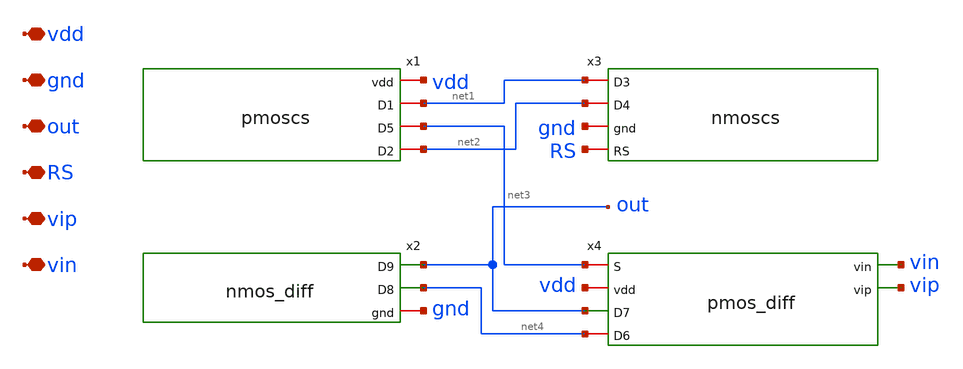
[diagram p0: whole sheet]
** sch_path: op_amp.sch
**.subckt op_amp vdd gnd out RS vip vin
*.iopin vdd
*.iopin gnd
*.iopin out
*.iopin RS
*.iopin vip
*.iopin vin
x1 vdd net1 net3 net2 pmoscs
x2 out net4 gnd nmos_diff
x4 net3 vin vip vdd out net4 pmos_diff
x3 net1 net2 gnd RS nmoscs
**.ends

* expanding   symbol:  pmoscs.sym # of pins=4
** sym_path: pmoscs.sym
** sch_path: pmoscs.sch
.subckt pmoscs vdd D1 D5 D2
*.iopin vdd
*.iopin D1
*.iopin D2
*.iopin D5
XM1 D1 D2 vdd vdd sky130_fd_pr__pfet_01v8 L=1 W=2 nf=1 ad='int((nf+1)/2) * W/nf * 0.29' as='int((nf+2)/2) * W/nf * 0.29'
+ pd='2*int((nf+1)/2) * (W/nf + 0.29)' ps='2*int((nf+2)/2) * (W/nf + 0.29)' nrd='0.29 / W' nrs='0.29 / W'
+ sa=0 sb=0 sd=0 mult=2 m=2
XM2 D2 D2 vdd vdd sky130_fd_pr__pfet_01v8 L=1 W=2 nf=1 ad='int((nf+1)/2) * W/nf * 0.29' as='int((nf+2)/2) * W/nf * 0.29'
+ pd='2*int((nf+1)/2) * (W/nf + 0.29)' ps='2*int((nf+2)/2) * (W/nf + 0.29)' nrd='0.29 / W' nrs='0.29 / W'
+ sa=0 sb=0 sd=0 mult=2 m=2
XM5 D5 D2 vdd vdd sky130_fd_pr__pfet_01v8 L=1 W=2 nf=1 ad='int((nf+1)/2) * W/nf * 0.29' as='int((nf+2)/2) * W/nf * 0.29'
+ pd='2*int((nf+1)/2) * (W/nf + 0.29)' ps='2*int((nf+2)/2) * (W/nf + 0.29)' nrd='0.29 / W' nrs='0.29 / W'
+ sa=0 sb=0 sd=0 mult=2 m=2
XM3 vdd vdd vdd vdd sky130_fd_pr__pfet_01v8 L=1 W=2 nf=1 ad='int((nf+1)/2) * W/nf * 0.29' as='int((nf+2)/2) * W/nf * 0.29'
+ pd='2*int((nf+1)/2) * (W/nf + 0.29)' ps='2*int((nf+2)/2) * (W/nf + 0.29)' nrd='0.29 / W' nrs='0.29 / W'
+ sa=0 sb=0 sd=0 mult=2 m=2
XM4 vdd vdd vdd vdd sky130_fd_pr__pfet_01v8 L=0.15 W=2 nf=1 ad='int((nf+1)/2) * W/nf * 0.29' as='int((nf+2)/2) * W/nf * 0.29'
+ pd='2*int((nf+1)/2) * (W/nf + 0.29)' ps='2*int((nf+2)/2) * (W/nf + 0.29)' nrd='0.29 / W' nrs='0.29 / W'
+ sa=0 sb=0 sd=0 mult=2 m=2
XM6 D2 D2 D2 vdd sky130_fd_pr__pfet_01v8 L=0.15 W=2 nf=1 ad='int((nf+1)/2) * W/nf * 0.29' as='int((nf+2)/2) * W/nf * 0.29'
+ pd='2*int((nf+1)/2) * (W/nf + 0.29)' ps='2*int((nf+2)/2) * (W/nf + 0.29)' nrd='0.29 / W' nrs='0.29 / W'
+ sa=0 sb=0 sd=0 mult=2 m=2
XM7 D1 D1 D1 vdd sky130_fd_pr__pfet_01v8 L=0.15 W=2 nf=1 ad='int((nf+1)/2) * W/nf * 0.29' as='int((nf+2)/2) * W/nf * 0.29'
+ pd='2*int((nf+1)/2) * (W/nf + 0.29)' ps='2*int((nf+2)/2) * (W/nf + 0.29)' nrd='0.29 / W' nrs='0.29 / W'
+ sa=0 sb=0 sd=0 mult=2 m=2
XM8 D5 D5 D5 vdd sky130_fd_pr__pfet_01v8 L=0.15 W=2 nf=1 ad='int((nf+1)/2) * W/nf * 0.29' as='int((nf+2)/2) * W/nf * 0.29'
+ pd='2*int((nf+1)/2) * (W/nf + 0.29)' ps='2*int((nf+2)/2) * (W/nf + 0.29)' nrd='0.29 / W' nrs='0.29 / W'
+ sa=0 sb=0 sd=0 mult=2 m=2
.ends


* expanding   symbol:  nmos_diff.sym # of pins=3
** sym_path: nmos_diff.sym
** sch_path: nmos_diff.sch
.subckt nmos_diff D9 D8 gnd
*.opin D9
*.iopin gnd
*.opin D8
XM8 D8 D8 gnd gnd sky130_fd_pr__nfet_01v8 L=0.8 W=1 nf=1 ad='int((nf+1)/2) * W/nf * 0.29' as='int((nf+2)/2) * W/nf * 0.29'
+ pd='2*int((nf+1)/2) * (W/nf + 0.29)' ps='2*int((nf+2)/2) * (W/nf + 0.29)' nrd='0.29 / W' nrs='0.29 / W'
+ sa=0 sb=0 sd=0 mult=4 m=4
XM9 D9 D8 gnd gnd sky130_fd_pr__nfet_01v8 L=0.8 W=1 nf=1 ad='int((nf+1)/2) * W/nf * 0.29' as='int((nf+2)/2) * W/nf * 0.29'
+ pd='2*int((nf+1)/2) * (W/nf + 0.29)' ps='2*int((nf+2)/2) * (W/nf + 0.29)' nrd='0.29 / W' nrs='0.29 / W'
+ sa=0 sb=0 sd=0 mult=4 m=4
XM2 D9 D9 D9 gnd sky130_fd_pr__nfet_01v8 L=0.15 W=1 nf=1 ad='int((nf+1)/2) * W/nf * 0.29' as='int((nf+2)/2) * W/nf * 0.29'
+ pd='2*int((nf+1)/2) * (W/nf + 0.29)' ps='2*int((nf+2)/2) * (W/nf + 0.29)' nrd='0.29 / W' nrs='0.29 / W'
+ sa=0 sb=0 sd=0 mult=2 m=2
XM1 D8 D8 D8 gnd sky130_fd_pr__nfet_01v8 L=0.15 W=1 nf=1 ad='int((nf+1)/2) * W/nf * 0.29' as='int((nf+2)/2) * W/nf * 0.29'
+ pd='2*int((nf+1)/2) * (W/nf + 0.29)' ps='2*int((nf+2)/2) * (W/nf + 0.29)' nrd='0.29 / W' nrs='0.29 / W'
+ sa=0 sb=0 sd=0 mult=2 m=2
.ends


* expanding   symbol:  pmos_diff.sym # of pins=6
** sym_path: pmos_diff.sym
** sch_path: pmos_diff.sch
.subckt pmos_diff S vin vip vdd D7 D6
*.ipin vin
*.ipin vip
*.opin D7
*.iopin D6
*.iopin vdd
*.iopin S
XM6 D6 vin S vdd sky130_fd_pr__pfet_01v8 L=0.5 W=1 nf=1 ad='int((nf+1)/2) * W/nf * 0.29' as='int((nf+2)/2) * W/nf * 0.29'
+ pd='2*int((nf+1)/2) * (W/nf + 0.29)' ps='2*int((nf+2)/2) * (W/nf + 0.29)' nrd='0.29 / W' nrs='0.29 / W'
+ sa=0 sb=0 sd=0 mult=4 m=4
XM7 D7 vip S vdd sky130_fd_pr__pfet_01v8 L=0.5 W=1 nf=1 ad='int((nf+1)/2) * W/nf * 0.29' as='int((nf+2)/2) * W/nf * 0.29'
+ pd='2*int((nf+1)/2) * (W/nf + 0.29)' ps='2*int((nf+2)/2) * (W/nf + 0.29)' nrd='0.29 / W' nrs='0.29 / W'
+ sa=0 sb=0 sd=0 mult=4 m=4
XM1 D6 D6 D6 vdd sky130_fd_pr__pfet_01v8 L=0.15 W=1 nf=1 ad='int((nf+1)/2) * W/nf * 0.29' as='int((nf+2)/2) * W/nf * 0.29'
+ pd='2*int((nf+1)/2) * (W/nf + 0.29)' ps='2*int((nf+2)/2) * (W/nf + 0.29)' nrd='0.29 / W' nrs='0.29 / W'
+ sa=0 sb=0 sd=0 mult=4 m=4
XM2 D7 D7 D7 vdd sky130_fd_pr__pfet_01v8 L=0.15 W=1 nf=1 ad='int((nf+1)/2) * W/nf * 0.29' as='int((nf+2)/2) * W/nf * 0.29'
+ pd='2*int((nf+1)/2) * (W/nf + 0.29)' ps='2*int((nf+2)/2) * (W/nf + 0.29)' nrd='0.29 / W' nrs='0.29 / W'
+ sa=0 sb=0 sd=0 mult=4 m=4
.ends


* expanding   symbol:  nmoscs.sym # of pins=4
** sym_path: nmoscs.sym
** sch_path: nmoscs.sch
.subckt nmoscs D3 D4 gnd RS
*.iopin RS
*.iopin D3
*.iopin D4
*.iopin gnd
XM3 D3 D3 gnd gnd sky130_fd_pr__nfet_01v8 L=1 W=2 nf=1 ad='int((nf+1)/2) * W/nf * 0.29' as='int((nf+2)/2) * W/nf * 0.29'
+ pd='2*int((nf+1)/2) * (W/nf + 0.29)' ps='2*int((nf+2)/2) * (W/nf + 0.29)' nrd='0.29 / W' nrs='0.29 / W'
+ sa=0 sb=0 sd=0 mult=2 m=2
XM4 D4 D3 RS gnd sky130_fd_pr__nfet_01v8 L=1 W=2 nf=1 ad='int((nf+1)/2) * W/nf * 0.29' as='int((nf+2)/2) * W/nf * 0.29'
+ pd='2*int((nf+1)/2) * (W/nf + 0.29)' ps='2*int((nf+2)/2) * (W/nf + 0.29)' nrd='0.29 / W' nrs='0.29 / W'
+ sa=0 sb=0 sd=0 mult=2 m=2
XM1 D3 D3 D3 gnd sky130_fd_pr__nfet_01v8 L=0.15u W=2u nf=1 ad='int((nf+1)/2) * W/nf * 0.29' as='int((nf+2)/2) * W/nf * 0.29'
+ pd='2*int((nf+1)/2) * (W/nf + 0.29)' ps='2*int((nf+2)/2) * (W/nf + 0.29)' nrd='0.29 / W' nrs='0.29 / W'
+ sa=0 sb=0 sd=0 mult=2 m=2
XM2 D4 D4 D4 gnd sky130_fd_pr__nfet_01v8 L=0.15u W=2u nf=1 ad='int((nf+1)/2) * W/nf * 0.29' as='int((nf+2)/2) * W/nf * 0.29'
+ pd='2*int((nf+1)/2) * (W/nf + 0.29)' ps='2*int((nf+2)/2) * (W/nf + 0.29)' nrd='0.29 / W' nrs='0.29 / W'
+ sa=0 sb=0 sd=0 mult=2 m=2
.ends

.end
